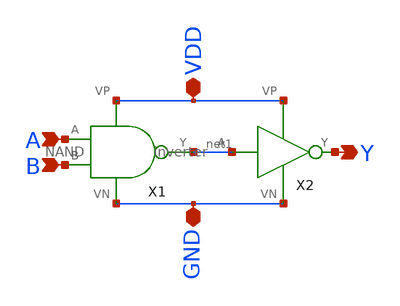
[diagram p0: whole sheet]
** sch_path: Miniproject1/AND.sch
**.subckt AND VDD GND A B Y
*.iopin VDD
*.iopin GND
*.ipin A
*.ipin B
*.opin Y
X1 A B net1 VDD GND NAND
X2 net1 Y VDD GND inverter
**.ends

* expanding   symbol:  /home/james/Documents/Miniproject1/NAND.sym # of pins=5
** sym_path: Miniproject1/NAND.sym
** sch_path: Miniproject1/NAND.sch
.subckt NAND A B Y VP VN
*.opin Y
*.ipin A
*.ipin B
*.iopin VP
*.iopin VN
XM1 VP B Y VDD sky130_fd_pr__pfet_01v8 L=0.15 W=1 nf=1 ad='int((nf+1)/2) * W/nf * 0.29' as='int((nf+2)/2) * W/nf * 0.29'
+ pd='2*int((nf+1)/2) * (W/nf + 0.29)' ps='2*int((nf+2)/2) * (W/nf + 0.29)' nrd='0.29 / W' nrs='0.29 / W'
+ sa=0 sb=0 sd=0 mult=1 m=1
XM2 Y A VP VDD sky130_fd_pr__pfet_01v8 L=0.15 W=1 nf=1 ad='int((nf+1)/2) * W/nf * 0.29' as='int((nf+2)/2) * W/nf * 0.29'
+ pd='2*int((nf+1)/2) * (W/nf + 0.29)' ps='2*int((nf+2)/2) * (W/nf + 0.29)' nrd='0.29 / W' nrs='0.29 / W'
+ sa=0 sb=0 sd=0 mult=1 m=1
XM3 Y A net1 GND sky130_fd_pr__nfet_01v8 L=0.15 W=1 nf=1 ad='int((nf+1)/2) * W/nf * 0.29' as='int((nf+2)/2) * W/nf * 0.29'
+ pd='2*int((nf+1)/2) * (W/nf + 0.29)' ps='2*int((nf+2)/2) * (W/nf + 0.29)' nrd='0.29 / W' nrs='0.29 / W'
+ sa=0 sb=0 sd=0 mult=1 m=1
XM4 VN B net1 GND sky130_fd_pr__nfet_01v8 L=0.15 W=1 nf=1 ad='int((nf+1)/2) * W/nf * 0.29' as='int((nf+2)/2) * W/nf * 0.29'
+ pd='2*int((nf+1)/2) * (W/nf + 0.29)' ps='2*int((nf+2)/2) * (W/nf + 0.29)' nrd='0.29 / W' nrs='0.29 / W'
+ sa=0 sb=0 sd=0 mult=1 m=1
.ends


* expanding   symbol:  /home/james/Documents/Miniproject1/inverter.sym # of pins=4
** sym_path: Miniproject1/inverter.sym
** sch_path: Miniproject1/inverter.sch
.subckt inverter A Y VP VN
*.ipin A
*.iopin VP
*.iopin VN
*.opin Y
XM2 Y A VP VDD sky130_fd_pr__pfet_01v8 L=0.15 W=1 nf=1 ad='int((nf+1)/2) * W/nf * 0.29' as='int((nf+2)/2) * W/nf * 0.29'
+ pd='2*int((nf+1)/2) * (W/nf + 0.29)' ps='2*int((nf+2)/2) * (W/nf + 0.29)' nrd='0.29 / W' nrs='0.29 / W'
+ sa=0 sb=0 sd=0 mult=1 m=1
XM1 Y A VN GND sky130_fd_pr__nfet_01v8 L=0.15 W=1 nf=1 ad='int((nf+1)/2) * W/nf * 0.29' as='int((nf+2)/2) * W/nf * 0.29'
+ pd='2*int((nf+1)/2) * (W/nf + 0.29)' ps='2*int((nf+2)/2) * (W/nf + 0.29)' nrd='0.29 / W' nrs='0.29 / W'
+ sa=0 sb=0 sd=0 mult=1 m=1
.ends

.end
